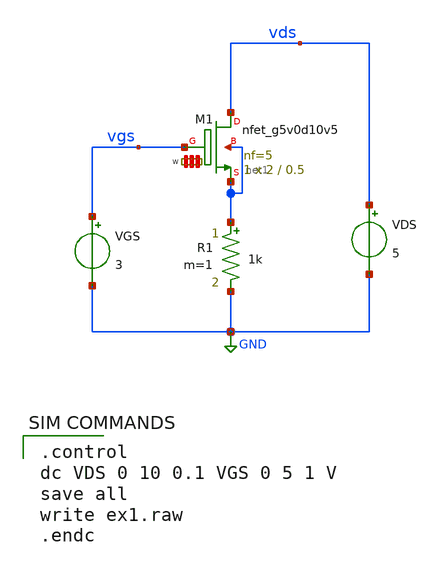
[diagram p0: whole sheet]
** sch_path: ex1.sch
**.subckt ex1
VGS vgs GND 3
VDS vds GND 5
R1 net1 GND 1k m=1
XM1 vds vgs net1 net1 sky130_fd_pr__nfet_g5v0d10v5 L=0.5 W='2 * 5 ' nf=5 ad='int((nf+1)/2) * W / nf * 0.29'
+ as='int((nf+2)/2) * W / nf * 0.29' pd='2*int((nf+1)/2) * (W / nf + 0.29)' ps='2*int((nf+2)/2) * (W / nf + 0.29)'
+ nrd='0.29 / W ' nrs='0.29 / W ' sa=0 sb=0 sd=0 mult=1 m=1
**** begin user architecture code

** opencircuitdesign pdks install
.lib $::SKYWATER_MODELS/sky130.lib.spice tt



.control
dc VDS 0 10 0.1 VGS 0 5 1 V
save all
write ex1.raw
.endc


**** end user architecture code
**.ends
.GLOBAL GND
.end
